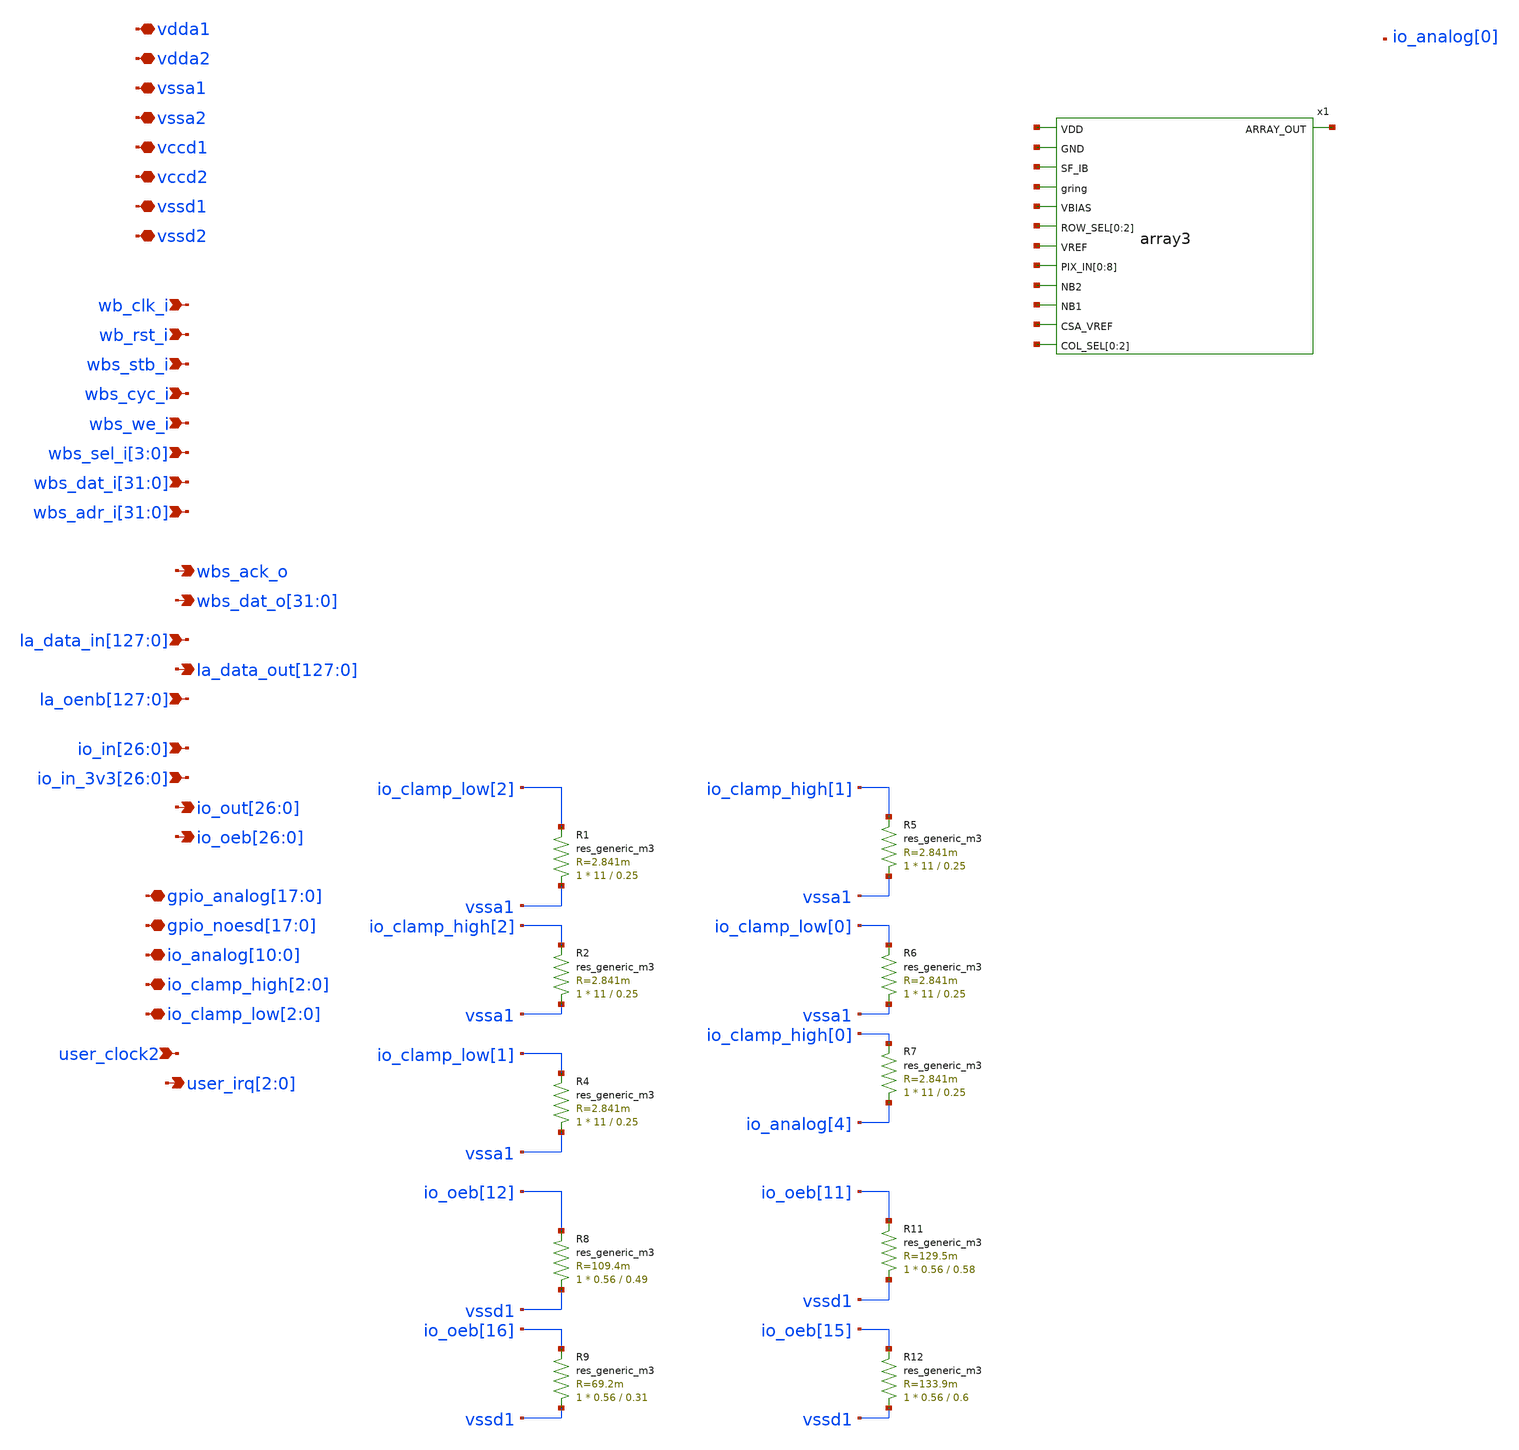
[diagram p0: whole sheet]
** sch_path: xschem/user_analog_project_wrapper.sch
**.subckt user_analog_project_wrapper vdda1 vdda2 vssa1 vssa2 vccd1 vccd2 vssd1 vssd2 wb_clk_i
*+ wb_rst_i wbs_stb_i wbs_cyc_i wbs_we_i wbs_sel_i[3],wbs_sel_i[2],wbs_sel_i[1],wbs_sel_i[0]
*+ wbs_dat_i[31],wbs_dat_i[30],wbs_dat_i[29],wbs_dat_i[28],wbs_dat_i[27],wbs_dat_i[26],wbs_dat_i[25],wbs_dat_i[24],wbs_dat_i[23],wbs_dat_i[22],wbs_dat_i[21],wbs_dat_i[20],wbs_dat_i[19],wbs_dat_i[18],wbs_dat_i[17],wbs_dat_i[16],wbs_dat_i[15],wbs_dat_i[14],wbs_dat_i[13],wbs_dat_i[12],wbs_dat_i[11],wbs_dat_i[10],wbs_dat_i[9],wbs_dat_i[8],wbs_dat_i[7],wbs_dat_i[6],wbs_dat_i[5],wbs_dat_i[4],wbs_dat_i[3],wbs_dat_i[2],wbs_dat_i[1],wbs_dat_i[0]
*+ wbs_adr_i[31],wbs_adr_i[30],wbs_adr_i[29],wbs_adr_i[28],wbs_adr_i[27],wbs_adr_i[26],wbs_adr_i[25],wbs_adr_i[24],wbs_adr_i[23],wbs_adr_i[22],wbs_adr_i[21],wbs_adr_i[20],wbs_adr_i[19],wbs_adr_i[18],wbs_adr_i[17],wbs_adr_i[16],wbs_adr_i[15],wbs_adr_i[14],wbs_adr_i[13],wbs_adr_i[12],wbs_adr_i[11],wbs_adr_i[10],wbs_adr_i[9],wbs_adr_i[8],wbs_adr_i[7],wbs_adr_i[6],wbs_adr_i[5],wbs_adr_i[4],wbs_adr_i[3],wbs_adr_i[2],wbs_adr_i[1],wbs_adr_i[0] wbs_ack_o
*+ wbs_dat_o[31],wbs_dat_o[30],wbs_dat_o[29],wbs_dat_o[28],wbs_dat_o[27],wbs_dat_o[26],wbs_dat_o[25],wbs_dat_o[24],wbs_dat_o[23],wbs_dat_o[22],wbs_dat_o[21],wbs_dat_o[20],wbs_dat_o[19],wbs_dat_o[18],wbs_dat_o[17],wbs_dat_o[16],wbs_dat_o[15],wbs_dat_o[14],wbs_dat_o[13],wbs_dat_o[12],wbs_dat_o[11],wbs_dat_o[10],wbs_dat_o[9],wbs_dat_o[8],wbs_dat_o[7],wbs_dat_o[6],wbs_dat_o[5],wbs_dat_o[4],wbs_dat_o[3],wbs_dat_o[2],wbs_dat_o[1],wbs_dat_o[0]
*+ la_data_in[127],la_data_in[126],la_data_in[125],la_data_in[124],la_data_in[123],la_data_in[122],la_data_in[121],la_data_in[120],la_data_in[119],la_data_in[118],la_data_in[117],la_data_in[116],la_data_in[115],la_data_in[114],la_data_in[113],la_data_in[112],la_data_in[111],la_data_in[110],la_data_in[109],la_data_in[108],la_data_in[107],la_data_in[106],la_data_in[105],la_data_in[104],la_data_in[103],la_data_in[102],la_data_in[101],la_data_in[100],la_data_in[99],la_data_in[98],la_data_in[97],la_data_in[96],la_data_in[95],la_data_in[94],la_data_in[93],la_data_in[92],la_data_in[91],la_data_in[90],la_data_in[89],la_data_in[88],la_data_in[87],la_data_in[86],la_data_in[85],la_data_in[84],la_data_in[83],la_data_in[82],la_data_in[81],la_data_in[80],la_data_in[79],la_data_in[78],la_data_in[77],la_data_in[76],la_data_in[75],la_data_in[74],la_data_in[73],la_data_in[72],la_data_in[71],la_data_in[70],la_data_in[69],la_data_in[68],la_data_in[67],la_data_in[66],la_data_in[65],la_data_in[64],la_data_in[63],la_data_in[62],la_data_in[61],la_data_in[60],la_data_in[59],la_data_in[58],la_data_in[57],la_data_in[56],la_data_in[55],la_data_in[54],la_data_in[53],la_data_in[52],la_data_in[51],la_data_in[50],la_data_in[49],la_data_in[48],la_data_in[47],la_data_in[46],la_data_in[45],la_data_in[44],la_data_in[43],la_data_in[42],la_data_in[41],la_data_in[40],la_data_in[39],la_data_in[38],la_data_in[37],la_data_in[36],la_data_in[35],la_data_in[34],la_data_in[33],la_data_in[32],la_data_in[31],la_data_in[30],la_data_in[29],la_data_in[28],la_data_in[27],la_data_in[26],la_data_in[25],la_data_in[24],la_data_in[23],la_data_in[22],la_data_in[21],la_data_in[20],la_data_in[19],la_data_in[18],la_data_in[17],la_data_in[16],la_data_in[15],la_data_in[14],la_data_in[13],la_data_in[12],la_data_in[11],la_data_in[10],la_data_in[9],la_data_in[8],la_data_in[7],la_data_in[6],la_data_in[5],la_data_in[4],la_data_in[3],la_data_in[2],la_data_in[1],la_data_in[0]
*+ la_data_out[127],la_data_out[126],la_data_out[125],la_data_out[124],la_data_out[123],la_data_out[122],la_data_out[121],la_data_out[120],la_data_out[119],la_data_out[118],la_data_out[117],la_data_out[116],la_data_out[115],la_data_out[114],la_data_out[113],la_data_out[112],la_data_out[111],la_data_out[110],la_data_out[109],la_data_out[108],la_data_out[107],la_data_out[106],la_data_out[105],la_data_out[104],la_data_out[103],la_data_out[102],la_data_out[101],la_data_out[100],la_data_out[99],la_data_out[98],la_data_out[97],la_data_out[96],la_data_out[95],la_data_out[94],la_data_out[93],la_data_out[92],la_data_out[91],la_data_out[90],la_data_out[89],la_data_out[88],la_data_out[87],la_data_out[86],la_data_out[85],la_data_out[84],la_data_out[83],la_data_out[82],la_data_out[81],la_data_out[80],la_data_out[79],la_data_out[78],la_data_out[77],la_data_out[76],la_data_out[75],la_data_out[74],la_data_out[73],la_data_out[72],la_data_out[71],la_data_out[70],la_data_out[69],la_data_out[68],la_data_out[67],la_data_out[66],la_data_out[65],la_data_out[64],la_data_out[63],la_data_out[62],la_data_out[61],la_data_out[60],la_data_out[59],la_data_out[58],la_data_out[57],la_data_out[56],la_data_out[55],la_data_out[54],la_data_out[53],la_data_out[52],la_data_out[51],la_data_out[50],la_data_out[49],la_data_out[48],la_data_out[47],la_data_out[46],la_data_out[45],la_data_out[44],la_data_out[43],la_data_out[42],la_data_out[41],la_data_out[40],la_data_out[39],la_data_out[38],la_data_out[37],la_data_out[36],la_data_out[35],la_data_out[34],la_data_out[33],la_data_out[32],la_data_out[31],la_data_out[30],la_data_out[29],la_data_out[28],la_data_out[27],la_data_out[26],la_data_out[25],la_data_out[24],la_data_out[23],la_data_out[22],la_data_out[21],la_data_out[20],la_data_out[19],la_data_out[18],la_data_out[17],la_data_out[16],la_data_out[15],la_data_out[14],la_data_out[13],la_data_out[12],la_data_out[11],la_data_out[10],la_data_out[9],la_data_out[8],la_data_out[7],la_data_out[6],la_data_out[5],la_data_out[4],la_data_out[3],la_data_out[2],la_data_out[1],la_data_out[0]
*+ io_in[26],io_in[25],io_in[24],io_in[23],io_in[22],io_in[21],io_in[20],io_in[19],io_in[18],io_in[17],io_in[16],io_in[15],io_in[14],io_in[13],io_in[12],io_in[11],io_in[10],io_in[9],io_in[8],io_in[7],io_in[6],io_in[5],io_in[4],io_in[3],io_in[2],io_in[1],io_in[0]
*+ io_in_3v3[26],io_in_3v3[25],io_in_3v3[24],io_in_3v3[23],io_in_3v3[22],io_in_3v3[21],io_in_3v3[20],io_in_3v3[19],io_in_3v3[18],io_in_3v3[17],io_in_3v3[16],io_in_3v3[15],io_in_3v3[14],io_in_3v3[13],io_in_3v3[12],io_in_3v3[11],io_in_3v3[10],io_in_3v3[9],io_in_3v3[8],io_in_3v3[7],io_in_3v3[6],io_in_3v3[5],io_in_3v3[4],io_in_3v3[3],io_in_3v3[2],io_in_3v3[1],io_in_3v3[0] user_clock2
*+ io_out[26],io_out[25],io_out[24],io_out[23],io_out[22],io_out[21],io_out[20],io_out[19],io_out[18],io_out[17],io_out[16],io_out[15],io_out[14],io_out[13],io_out[12],io_out[11],io_out[10],io_out[9],io_out[8],io_out[7],io_out[6],io_out[5],io_out[4],io_out[3],io_out[2],io_out[1],io_out[0]
*+ io_oeb[26],io_oeb[25],io_oeb[24],io_oeb[23],io_oeb[22],io_oeb[21],io_oeb[20],io_oeb[19],io_oeb[18],io_oeb[17],io_oeb[16],io_oeb[15],io_oeb[14],io_oeb[13],io_oeb[12],io_oeb[11],io_oeb[10],io_oeb[9],io_oeb[8],io_oeb[7],io_oeb[6],io_oeb[5],io_oeb[4],io_oeb[3],io_oeb[2],io_oeb[1],io_oeb[0]
*+ gpio_analog[17],gpio_analog[16],gpio_analog[15],gpio_analog[14],gpio_analog[13],gpio_analog[12],gpio_analog[11],gpio_analog[10],gpio_analog[9],gpio_analog[8],gpio_analog[7],gpio_analog[6],gpio_analog[5],gpio_analog[4],gpio_analog[3],gpio_analog[2],gpio_analog[1],gpio_analog[0]
*+ gpio_noesd[17],gpio_noesd[16],gpio_noesd[15],gpio_noesd[14],gpio_noesd[13],gpio_noesd[12],gpio_noesd[11],gpio_noesd[10],gpio_noesd[9],gpio_noesd[8],gpio_noesd[7],gpio_noesd[6],gpio_noesd[5],gpio_noesd[4],gpio_noesd[3],gpio_noesd[2],gpio_noesd[1],gpio_noesd[0]
*+ io_analog[10],io_analog[9],io_analog[8],io_analog[7],io_analog[6],io_analog[5],io_analog[4],io_analog[3],io_analog[2],io_analog[1],io_analog[0] io_clamp_high[2],io_clamp_high[1],io_clamp_high[0] io_clamp_low[2],io_clamp_low[1],io_clamp_low[0]
*+ user_irq[2],user_irq[1],user_irq[0]
*+ la_oenb[127],la_oenb[126],la_oenb[125],la_oenb[124],la_oenb[123],la_oenb[122],la_oenb[121],la_oenb[120],la_oenb[119],la_oenb[118],la_oenb[117],la_oenb[116],la_oenb[115],la_oenb[114],la_oenb[113],la_oenb[112],la_oenb[111],la_oenb[110],la_oenb[109],la_oenb[108],la_oenb[107],la_oenb[106],la_oenb[105],la_oenb[104],la_oenb[103],la_oenb[102],la_oenb[101],la_oenb[100],la_oenb[99],la_oenb[98],la_oenb[97],la_oenb[96],la_oenb[95],la_oenb[94],la_oenb[93],la_oenb[92],la_oenb[91],la_oenb[90],la_oenb[89],la_oenb[88],la_oenb[87],la_oenb[86],la_oenb[85],la_oenb[84],la_oenb[83],la_oenb[82],la_oenb[81],la_oenb[80],la_oenb[79],la_oenb[78],la_oenb[77],la_oenb[76],la_oenb[75],la_oenb[74],la_oenb[73],la_oenb[72],la_oenb[71],la_oenb[70],la_oenb[69],la_oenb[68],la_oenb[67],la_oenb[66],la_oenb[65],la_oenb[64],la_oenb[63],la_oenb[62],la_oenb[61],la_oenb[60],la_oenb[59],la_oenb[58],la_oenb[57],la_oenb[56],la_oenb[55],la_oenb[54],la_oenb[53],la_oenb[52],la_oenb[51],la_oenb[50],la_oenb[49],la_oenb[48],la_oenb[47],la_oenb[46],la_oenb[45],la_oenb[44],la_oenb[43],la_oenb[42],la_oenb[41],la_oenb[40],la_oenb[39],la_oenb[38],la_oenb[37],la_oenb[36],la_oenb[35],la_oenb[34],la_oenb[33],la_oenb[32],la_oenb[31],la_oenb[30],la_oenb[29],la_oenb[28],la_oenb[27],la_oenb[26],la_oenb[25],la_oenb[24],la_oenb[23],la_oenb[22],la_oenb[21],la_oenb[20],la_oenb[19],la_oenb[18],la_oenb[17],la_oenb[16],la_oenb[15],la_oenb[14],la_oenb[13],la_oenb[12],la_oenb[11],la_oenb[10],la_oenb[9],la_oenb[8],la_oenb[7],la_oenb[6],la_oenb[5],la_oenb[4],la_oenb[3],la_oenb[2],la_oenb[1],la_oenb[0]
*.iopin vdda1
*.iopin vdda2
*.iopin vssa1
*.iopin vssa2
*.iopin vccd1
*.iopin vccd2
*.iopin vssd1
*.iopin vssd2
*.ipin wb_clk_i
*.ipin wb_rst_i
*.ipin wbs_stb_i
*.ipin wbs_cyc_i
*.ipin wbs_we_i
*.ipin wbs_sel_i[3],wbs_sel_i[2],wbs_sel_i[1],wbs_sel_i[0]
*.ipin
*+ wbs_dat_i[31],wbs_dat_i[30],wbs_dat_i[29],wbs_dat_i[28],wbs_dat_i[27],wbs_dat_i[26],wbs_dat_i[25],wbs_dat_i[24],wbs_dat_i[23],wbs_dat_i[22],wbs_dat_i[21],wbs_dat_i[20],wbs_dat_i[19],wbs_dat_i[18],wbs_dat_i[17],wbs_dat_i[16],wbs_dat_i[15],wbs_dat_i[14],wbs_dat_i[13],wbs_dat_i[12],wbs_dat_i[11],wbs_dat_i[10],wbs_dat_i[9],wbs_dat_i[8],wbs_dat_i[7],wbs_dat_i[6],wbs_dat_i[5],wbs_dat_i[4],wbs_dat_i[3],wbs_dat_i[2],wbs_dat_i[1],wbs_dat_i[0]
*.ipin
*+ wbs_adr_i[31],wbs_adr_i[30],wbs_adr_i[29],wbs_adr_i[28],wbs_adr_i[27],wbs_adr_i[26],wbs_adr_i[25],wbs_adr_i[24],wbs_adr_i[23],wbs_adr_i[22],wbs_adr_i[21],wbs_adr_i[20],wbs_adr_i[19],wbs_adr_i[18],wbs_adr_i[17],wbs_adr_i[16],wbs_adr_i[15],wbs_adr_i[14],wbs_adr_i[13],wbs_adr_i[12],wbs_adr_i[11],wbs_adr_i[10],wbs_adr_i[9],wbs_adr_i[8],wbs_adr_i[7],wbs_adr_i[6],wbs_adr_i[5],wbs_adr_i[4],wbs_adr_i[3],wbs_adr_i[2],wbs_adr_i[1],wbs_adr_i[0]
*.opin wbs_ack_o
*.opin
*+ wbs_dat_o[31],wbs_dat_o[30],wbs_dat_o[29],wbs_dat_o[28],wbs_dat_o[27],wbs_dat_o[26],wbs_dat_o[25],wbs_dat_o[24],wbs_dat_o[23],wbs_dat_o[22],wbs_dat_o[21],wbs_dat_o[20],wbs_dat_o[19],wbs_dat_o[18],wbs_dat_o[17],wbs_dat_o[16],wbs_dat_o[15],wbs_dat_o[14],wbs_dat_o[13],wbs_dat_o[12],wbs_dat_o[11],wbs_dat_o[10],wbs_dat_o[9],wbs_dat_o[8],wbs_dat_o[7],wbs_dat_o[6],wbs_dat_o[5],wbs_dat_o[4],wbs_dat_o[3],wbs_dat_o[2],wbs_dat_o[1],wbs_dat_o[0]
*.ipin
*+ la_data_in[127],la_data_in[126],la_data_in[125],la_data_in[124],la_data_in[123],la_data_in[122],la_data_in[121],la_data_in[120],la_data_in[119],la_data_in[118],la_data_in[117],la_data_in[116],la_data_in[115],la_data_in[114],la_data_in[113],la_data_in[112],la_data_in[111],la_data_in[110],la_data_in[109],la_data_in[108],la_data_in[107],la_data_in[106],la_data_in[105],la_data_in[104],la_data_in[103],la_data_in[102],la_data_in[101],la_data_in[100],la_data_in[99],la_data_in[98],la_data_in[97],la_data_in[96],la_data_in[95],la_data_in[94],la_data_in[93],la_data_in[92],la_data_in[91],la_data_in[90],la_data_in[89],la_data_in[88],la_data_in[87],la_data_in[86],la_data_in[85],la_data_in[84],la_data_in[83],la_data_in[82],la_data_in[81],la_data_in[80],la_data_in[79],la_data_in[78],la_data_in[77],la_data_in[76],la_data_in[75],la_data_in[74],la_data_in[73],la_data_in[72],la_data_in[71],la_data_in[70],la_data_in[69],la_data_in[68],la_data_in[67],la_data_in[66],la_data_in[65],la_data_in[64],la_data_in[63],la_data_in[62],la_data_in[61],la_data_in[60],la_data_in[59],la_data_in[58],la_data_in[57],la_data_in[56],la_data_in[55],la_data_in[54],la_data_in[53],la_data_in[52],la_data_in[51],la_data_in[50],la_data_in[49],la_data_in[48],la_data_in[47],la_data_in[46],la_data_in[45],la_data_in[44],la_data_in[43],la_data_in[42],la_data_in[41],la_data_in[40],la_data_in[39],la_data_in[38],la_data_in[37],la_data_in[36],la_data_in[35],la_data_in[34],la_data_in[33],la_data_in[32],la_data_in[31],la_data_in[30],la_data_in[29],la_data_in[28],la_data_in[27],la_data_in[26],la_data_in[25],la_data_in[24],la_data_in[23],la_data_in[22],la_data_in[21],la_data_in[20],la_data_in[19],la_data_in[18],la_data_in[17],la_data_in[16],la_data_in[15],la_data_in[14],la_data_in[13],la_data_in[12],la_data_in[11],la_data_in[10],la_data_in[9],la_data_in[8],la_data_in[7],la_data_in[6],la_data_in[5],la_data_in[4],la_data_in[3],la_data_in[2],la_data_in[1],la_data_in[0]
*.opin
*+ la_data_out[127],la_data_out[126],la_data_out[125],la_data_out[124],la_data_out[123],la_data_out[122],la_data_out[121],la_data_out[120],la_data_out[119],la_data_out[118],la_data_out[117],la_data_out[116],la_data_out[115],la_data_out[114],la_data_out[113],la_data_out[112],la_data_out[111],la_data_out[110],la_data_out[109],la_data_out[108],la_data_out[107],la_data_out[106],la_data_out[105],la_data_out[104],la_data_out[103],la_data_out[102],la_data_out[101],la_data_out[100],la_data_out[99],la_data_out[98],la_data_out[97],la_data_out[96],la_data_out[95],la_data_out[94],la_data_out[93],la_data_out[92],la_data_out[91],la_data_out[90],la_data_out[89],la_data_out[88],la_data_out[87],la_data_out[86],la_data_out[85],la_data_out[84],la_data_out[83],la_data_out[82],la_data_out[81],la_data_out[80],la_data_out[79],la_data_out[78],la_data_out[77],la_data_out[76],la_data_out[75],la_data_out[74],la_data_out[73],la_data_out[72],la_data_out[71],la_data_out[70],la_data_out[69],la_data_out[68],la_data_out[67],la_data_out[66],la_data_out[65],la_data_out[64],la_data_out[63],la_data_out[62],la_data_out[61],la_data_out[60],la_data_out[59],la_data_out[58],la_data_out[57],la_data_out[56],la_data_out[55],la_data_out[54],la_data_out[53],la_data_out[52],la_data_out[51],la_data_out[50],la_data_out[49],la_data_out[48],la_data_out[47],la_data_out[46],la_data_out[45],la_data_out[44],la_data_out[43],la_data_out[42],la_data_out[41],la_data_out[40],la_data_out[39],la_data_out[38],la_data_out[37],la_data_out[36],la_data_out[35],la_data_out[34],la_data_out[33],la_data_out[32],la_data_out[31],la_data_out[30],la_data_out[29],la_data_out[28],la_data_out[27],la_data_out[26],la_data_out[25],la_data_out[24],la_data_out[23],la_data_out[22],la_data_out[21],la_data_out[20],la_data_out[19],la_data_out[18],la_data_out[17],la_data_out[16],la_data_out[15],la_data_out[14],la_data_out[13],la_data_out[12],la_data_out[11],la_data_out[10],la_data_out[9],la_data_out[8],la_data_out[7],la_data_out[6],la_data_out[5],la_data_out[4],la_data_out[3],la_data_out[2],la_data_out[1],la_data_out[0]
*.ipin
*+ io_in[26],io_in[25],io_in[24],io_in[23],io_in[22],io_in[21],io_in[20],io_in[19],io_in[18],io_in[17],io_in[16],io_in[15],io_in[14],io_in[13],io_in[12],io_in[11],io_in[10],io_in[9],io_in[8],io_in[7],io_in[6],io_in[5],io_in[4],io_in[3],io_in[2],io_in[1],io_in[0]
*.ipin
*+ io_in_3v3[26],io_in_3v3[25],io_in_3v3[24],io_in_3v3[23],io_in_3v3[22],io_in_3v3[21],io_in_3v3[20],io_in_3v3[19],io_in_3v3[18],io_in_3v3[17],io_in_3v3[16],io_in_3v3[15],io_in_3v3[14],io_in_3v3[13],io_in_3v3[12],io_in_3v3[11],io_in_3v3[10],io_in_3v3[9],io_in_3v3[8],io_in_3v3[7],io_in_3v3[6],io_in_3v3[5],io_in_3v3[4],io_in_3v3[3],io_in_3v3[2],io_in_3v3[1],io_in_3v3[0]
*.ipin user_clock2
*.opin
*+ io_out[26],io_out[25],io_out[24],io_out[23],io_out[22],io_out[21],io_out[20],io_out[19],io_out[18],io_out[17],io_out[16],io_out[15],io_out[14],io_out[13],io_out[12],io_out[11],io_out[10],io_out[9],io_out[8],io_out[7],io_out[6],io_out[5],io_out[4],io_out[3],io_out[2],io_out[1],io_out[0]
*.opin
*+ io_oeb[26],io_oeb[25],io_oeb[24],io_oeb[23],io_oeb[22],io_oeb[21],io_oeb[20],io_oeb[19],io_oeb[18],io_oeb[17],io_oeb[16],io_oeb[15],io_oeb[14],io_oeb[13],io_oeb[12],io_oeb[11],io_oeb[10],io_oeb[9],io_oeb[8],io_oeb[7],io_oeb[6],io_oeb[5],io_oeb[4],io_oeb[3],io_oeb[2],io_oeb[1],io_oeb[0]
*.iopin
*+ gpio_analog[17],gpio_analog[16],gpio_analog[15],gpio_analog[14],gpio_analog[13],gpio_analog[12],gpio_analog[11],gpio_analog[10],gpio_analog[9],gpio_analog[8],gpio_analog[7],gpio_analog[6],gpio_analog[5],gpio_analog[4],gpio_analog[3],gpio_analog[2],gpio_analog[1],gpio_analog[0]
*.iopin
*+ gpio_noesd[17],gpio_noesd[16],gpio_noesd[15],gpio_noesd[14],gpio_noesd[13],gpio_noesd[12],gpio_noesd[11],gpio_noesd[10],gpio_noesd[9],gpio_noesd[8],gpio_noesd[7],gpio_noesd[6],gpio_noesd[5],gpio_noesd[4],gpio_noesd[3],gpio_noesd[2],gpio_noesd[1],gpio_noesd[0]
*.iopin
*+ io_analog[10],io_analog[9],io_analog[8],io_analog[7],io_analog[6],io_analog[5],io_analog[4],io_analog[3],io_analog[2],io_analog[1],io_analog[0]
*.iopin io_clamp_high[2],io_clamp_high[1],io_clamp_high[0]
*.iopin io_clamp_low[2],io_clamp_low[1],io_clamp_low[0]
*.opin user_irq[2],user_irq[1],user_irq[0]
*.ipin
*+ la_oenb[127],la_oenb[126],la_oenb[125],la_oenb[124],la_oenb[123],la_oenb[122],la_oenb[121],la_oenb[120],la_oenb[119],la_oenb[118],la_oenb[117],la_oenb[116],la_oenb[115],la_oenb[114],la_oenb[113],la_oenb[112],la_oenb[111],la_oenb[110],la_oenb[109],la_oenb[108],la_oenb[107],la_oenb[106],la_oenb[105],la_oenb[104],la_oenb[103],la_oenb[102],la_oenb[101],la_oenb[100],la_oenb[99],la_oenb[98],la_oenb[97],la_oenb[96],la_oenb[95],la_oenb[94],la_oenb[93],la_oenb[92],la_oenb[91],la_oenb[90],la_oenb[89],la_oenb[88],la_oenb[87],la_oenb[86],la_oenb[85],la_oenb[84],la_oenb[83],la_oenb[82],la_oenb[81],la_oenb[80],la_oenb[79],la_oenb[78],la_oenb[77],la_oenb[76],la_oenb[75],la_oenb[74],la_oenb[73],la_oenb[72],la_oenb[71],la_oenb[70],la_oenb[69],la_oenb[68],la_oenb[67],la_oenb[66],la_oenb[65],la_oenb[64],la_oenb[63],la_oenb[62],la_oenb[61],la_oenb[60],la_oenb[59],la_oenb[58],la_oenb[57],la_oenb[56],la_oenb[55],la_oenb[54],la_oenb[53],la_oenb[52],la_oenb[51],la_oenb[50],la_oenb[49],la_oenb[48],la_oenb[47],la_oenb[46],la_oenb[45],la_oenb[44],la_oenb[43],la_oenb[42],la_oenb[41],la_oenb[40],la_oenb[39],la_oenb[38],la_oenb[37],la_oenb[36],la_oenb[35],la_oenb[34],la_oenb[33],la_oenb[32],la_oenb[31],la_oenb[30],la_oenb[29],la_oenb[28],la_oenb[27],la_oenb[26],la_oenb[25],la_oenb[24],la_oenb[23],la_oenb[22],la_oenb[21],la_oenb[20],la_oenb[19],la_oenb[18],la_oenb[17],la_oenb[16],la_oenb[15],la_oenb[14],la_oenb[13],la_oenb[12],la_oenb[11],la_oenb[10],la_oenb[9],la_oenb[8],la_oenb[7],la_oenb[6],la_oenb[5],la_oenb[4],la_oenb[3],la_oenb[2],la_oenb[1],la_oenb[0]
R1 vssa1 io_clamp_low[2] sky130_fd_pr__res_generic_m3 W=11 L=0.25 m=1
R2 vssa1 io_clamp_high[2] sky130_fd_pr__res_generic_m3 W=11 L=0.25 m=1
R4 vssa1 io_clamp_low[1] sky130_fd_pr__res_generic_m3 W=11 L=0.25 m=1
R5 vssa1 io_clamp_high[1] sky130_fd_pr__res_generic_m3 W=11 L=0.25 m=1
R6 vssa1 io_clamp_low[0] sky130_fd_pr__res_generic_m3 W=11 L=0.25 m=1
R7 io_analog[4] io_clamp_high[0] sky130_fd_pr__res_generic_m3 W=11 L=0.25 m=1
R8 vssd1 io_oeb[12] sky130_fd_pr__res_generic_m3 W=0.56 L=0.49 m=1
R9 vssd1 io_oeb[16] sky130_fd_pr__res_generic_m3 W=0.56 L=0.31 m=1
R11 vssd1 io_oeb[11] sky130_fd_pr__res_generic_m3 W=0.56 L=0.58 m=1
R12 vssd1 io_oeb[15] sky130_fd_pr__res_generic_m3 W=0.56 L=0.6 m=1
x1 net1 net2 net3 net4 net5 net6 net7[2] net7[1] net7[0] net8 net9[8] net9[7] net9[6] net9[5]
+ net9[4] net9[3] net9[2] net9[1] net9[0] net10 net11 net12 net13[2] net13[1] net13[0] array3
**.ends

* expanding   symbol:  array3.sym # of pins=13
** sym_path: xschem/array3.sym
** sch_path: xschem/array3.sch
.subckt array3 VDD GND SF_IB gring VBIAS ARRAY_OUT ROW_SEL[0] ROW_SEL[1] ROW_SEL[2] VREF PIX_IN[0]
+ PIX_IN[1] PIX_IN[2] PIX_IN[3] PIX_IN[4] PIX_IN[5] PIX_IN[6] PIX_IN[7] PIX_IN[8] NB2 NB1 CSA_VREF COL_SEL[0]
+ COL_SEL[1] COL_SEL[2]
*.ipin VDD
*.ipin GND
*.ipin SF_IB
*.ipin gring
*.ipin VBIAS
*.opin ARRAY_OUT
*.ipin ROW_SEL[0],ROW_SEL[1],ROW_SEL[2]
*.ipin VREF
*.ipin PIX_IN[0],PIX_IN[1],PIX_IN[2],PIX_IN[3],PIX_IN[4],PIX_IN[5],PIX_IN[6],PIX_IN[7],PIX_IN[8]
*.ipin NB2
*.ipin NB1
*.ipin CSA_VREF
*.ipin COL_SEL[0],COL_SEL[1],COL_SEL[2]
xPix0 VDD GND SF_IB gring VBIAS COL_OUT[0] ROW_SEL[0] VREF PIX_IN[0] NB2 NB1 CSA_VREF pixel
xPix1 VDD GND SF_IB gring VBIAS COL_OUT[1] ROW_SEL[0] VREF PIX_IN[1] NB2 NB1 CSA_VREF pixel
xPix2 VDD GND SF_IB gring VBIAS COL_OUT[2] ROW_SEL[0] VREF PIX_IN[2] NB2 NB1 CSA_VREF pixel
xPix3 VDD GND SF_IB gring VBIAS COL_OUT[0] ROW_SEL[1] VREF PIX_IN[3] NB2 NB1 CSA_VREF pixel
xPix4 VDD GND SF_IB gring VBIAS COL_OUT[1] ROW_SEL[1] VREF PIX_IN[4] NB2 NB1 CSA_VREF pixel
xPix5 VDD GND SF_IB gring VBIAS COL_OUT[2] ROW_SEL[1] VREF PIX_IN[5] NB2 NB1 CSA_VREF pixel
xPix6 VDD GND SF_IB gring VBIAS COL_OUT[0] ROW_SEL[2] VREF PIX_IN[6] NB2 NB1 CSA_VREF pixel
xPix7 VDD GND SF_IB gring VBIAS COL_OUT[1] ROW_SEL[2] VREF PIX_IN[7] NB2 NB1 CSA_VREF pixel
xPix8 VDD GND SF_IB gring VBIAS COL_OUT[2] ROW_SEL[2] VREF PIX_IN[8] NB2 NB1 CSA_VREF pixel
XM0 COL_OUT[0] COL_SEL[0] ARRAY_OUT GND sky130_fd_pr__nfet_01v8_lvt L=2 W=8 nf=1 ad='int((nf+1)/2) * W/nf * 0.29'
+ as='int((nf+2)/2) * W/nf * 0.29' pd='2*int((nf+1)/2) * (W/nf + 0.29)' ps='2*int((nf+2)/2) * (W/nf + 0.29)'
+ nrd='0.29 / W' nrs='0.29 / W' sa=0 sb=0 sd=0 mult=1 m=1
XM1 COL_OUT[1] COL_SEL[1] ARRAY_OUT GND sky130_fd_pr__nfet_01v8_lvt L=2 W=8 nf=1 ad='int((nf+1)/2) * W/nf * 0.29'
+ as='int((nf+2)/2) * W/nf * 0.29' pd='2*int((nf+1)/2) * (W/nf + 0.29)' ps='2*int((nf+2)/2) * (W/nf + 0.29)'
+ nrd='0.29 / W' nrs='0.29 / W' sa=0 sb=0 sd=0 mult=1 m=1
XM2 COL_OUT[2] COL_SEL[2] ARRAY_OUT GND sky130_fd_pr__nfet_01v8_lvt L=2 W=8 nf=1 ad='int((nf+1)/2) * W/nf * 0.29'
+ as='int((nf+2)/2) * W/nf * 0.29' pd='2*int((nf+1)/2) * (W/nf + 0.29)' ps='2*int((nf+2)/2) * (W/nf + 0.29)'
+ nrd='0.29 / W' nrs='0.29 / W' sa=0 sb=0 sd=0 mult=1 m=1
.ends


* expanding   symbol:  pixel/pixel.sym # of pins=12
** sym_path: xschem/pixel/pixel.sym
** sch_path: xschem/pixel/pixel.sch
.subckt pixel VDD GND SF_IB gring VBIAS pix_out ROW_SEL VREF AMP_IN NB2 NB1 CSA_VREF
*.opin pix_out
*.ipin SF_IB
*.ipin ROW_SEL
*.ipin VREF
*.ipin AMP_IN
*.ipin NB1
*.ipin CSA_VREF
*.ipin VBIAS
*.ipin NB2
*.ipin VDD
*.ipin GND
*.ipin gring
XM2 net2 ROW_SEL pix_out GND sky130_fd_pr__nfet_01v8_lvt L=1 W=2 nf=1 ad='int((nf+1)/2) * W/nf * 0.29'
+ as='int((nf+2)/2) * W/nf * 0.29' pd='2*int((nf+1)/2) * (W/nf + 0.29)' ps='2*int((nf+2)/2) * (W/nf + 0.29)'
+ nrd='0.29 / W' nrs='0.29 / W' sa=0 sb=0 sd=0 mult=1 m=1
XM3 GND AMP_OUT net1 VDD sky130_fd_pr__pfet_01v8_lvt L=1 W=1 nf=1 ad='int((nf+1)/2) * W/nf * 0.29' as='int((nf+2)/2) * W/nf * 0.29'
+ pd='2*int((nf+1)/2) * (W/nf + 0.29)' ps='2*int((nf+2)/2) * (W/nf + 0.29)' nrd='0.29 / W' nrs='0.29 / W'
+ sa=0 sb=0 sd=0 mult=1 m=1
XM5 net1 SF_IB VDD VDD sky130_fd_pr__pfet_01v8_lvt L=1 W=1 nf=1 ad='int((nf+1)/2) * W/nf * 0.29' as='int((nf+2)/2) * W/nf * 0.29'
+ pd='2*int((nf+1)/2) * (W/nf + 0.29)' ps='2*int((nf+2)/2) * (W/nf + 0.29)' nrd='0.29 / W' nrs='0.29 / W'
+ sa=0 sb=0 sd=0 mult=1 m=1
XM7 VDD net1 net2 GND sky130_fd_pr__nfet_01v8_lvt L=0.15 W=1 nf=1 ad='int((nf+1)/2) * W/nf * 0.29' as='int((nf+2)/2) * W/nf * 0.29'
+ pd='2*int((nf+1)/2) * (W/nf + 0.29)' ps='2*int((nf+2)/2) * (W/nf + 0.29)' nrd='0.29 / W' nrs='0.29 / W'
+ sa=0 sb=0 sd=0 mult=1 m=1
XM1 VDD net6 AMP_OUT GND sky130_fd_pr__nfet_01v8_lvt L=1 W=1 nf=1 ad='int((nf+1)/2) * W/nf * 0.29' as='int((nf+2)/2) * W/nf * 0.29'
+ pd='2*int((nf+1)/2) * (W/nf + 0.29)' ps='2*int((nf+2)/2) * (W/nf + 0.29)' nrd='0.29 / W' nrs='0.29 / W'
+ sa=0 sb=0 sd=0 mult=1 m=1
XM8 net5 net5 net7 VDD sky130_fd_pr__pfet_01v8_lvt L=2 W=1 nf=1 ad='int((nf+1)/2) * W/nf * 0.29' as='int((nf+2)/2) * W/nf * 0.29'
+ pd='2*int((nf+1)/2) * (W/nf + 0.29)' ps='2*int((nf+2)/2) * (W/nf + 0.29)' nrd='0.29 / W' nrs='0.29 / W'
+ sa=0 sb=0 sd=0 mult=1 m=1
XM10 net8 net7 VDD VDD sky130_fd_pr__pfet_01v8_lvt L=2 W=1 nf=1 ad='int((nf+1)/2) * W/nf * 0.29' as='int((nf+2)/2) * W/nf * 0.29'
+ pd='2*int((nf+1)/2) * (W/nf + 0.29)' ps='2*int((nf+2)/2) * (W/nf + 0.29)' nrd='0.29 / W' nrs='0.29 / W'
+ sa=0 sb=0 sd=0 mult=1 m=1
XM11 net7 net7 VDD VDD sky130_fd_pr__pfet_01v8_lvt L=2 W=1 nf=1 ad='int((nf+1)/2) * W/nf * 0.29' as='int((nf+2)/2) * W/nf * 0.29'
+ pd='2*int((nf+1)/2) * (W/nf + 0.29)' ps='2*int((nf+2)/2) * (W/nf + 0.29)' nrd='0.29 / W' nrs='0.29 / W'
+ sa=0 sb=0 sd=0 mult=1 m=1
XM15 AMP_OUT NB2 GND GND sky130_fd_pr__nfet_01v8_lvt L=1.15 W=1 nf=1 ad='int((nf+1)/2) * W/nf * 0.29'
+ as='int((nf+2)/2) * W/nf * 0.29' pd='2*int((nf+1)/2) * (W/nf + 0.29)' ps='2*int((nf+2)/2) * (W/nf + 0.29)'
+ nrd='0.29 / W' nrs='0.29 / W' sa=0 sb=0 sd=0 mult=1 m=1
XM16 net4 NB1 GND GND sky130_fd_pr__nfet_01v8_lvt L=1 W=1.2 nf=1 ad='int((nf+1)/2) * W/nf * 0.29' as='int((nf+2)/2) * W/nf * 0.29'
+ pd='2*int((nf+1)/2) * (W/nf + 0.29)' ps='2*int((nf+2)/2) * (W/nf + 0.29)' nrd='0.29 / W' nrs='0.29 / W'
+ sa=0 sb=0 sd=0 mult=1 m=1
XC3 AMP_IN AMP_OUT sky130_fd_pr__cap_mim_m3_1 W=2 L=2 MF=1 m=1
XM4 net3 VREF net4 GND sky130_fd_pr__nfet_01v8_lvt L=0.15 W=7 nf=1 ad='int((nf+1)/2) * W/nf * 0.29' as='int((nf+2)/2) * W/nf * 0.29'
+ pd='2*int((nf+1)/2) * (W/nf + 0.29)' ps='2*int((nf+2)/2) * (W/nf + 0.29)' nrd='0.29 / W' nrs='0.29 / W'
+ sa=0 sb=0 sd=0 mult=1 m=1
XM6 AMP_IN CSA_VREF AMP_OUT VDD sky130_fd_pr__pfet_01v8_lvt L=7.95 W=0.42 nf=1 ad='int((nf+1)/2) * W/nf * 0.29'
+ as='int((nf+2)/2) * W/nf * 0.29' pd='2*int((nf+1)/2) * (W/nf + 0.29)' ps='2*int((nf+2)/2) * (W/nf + 0.29)'
+ nrd='0.29 / W' nrs='0.29 / W' sa=0 sb=0 sd=0 mult=1 m=1
XM9 net6 net5 net8 VDD sky130_fd_pr__pfet_01v8_lvt L=2 W=1 nf=1 ad='int((nf+1)/2) * W/nf * 0.29' as='int((nf+2)/2) * W/nf * 0.29'
+ pd='2*int((nf+1)/2) * (W/nf + 0.29)' ps='2*int((nf+2)/2) * (W/nf + 0.29)' nrd='0.29 / W' nrs='0.29 / W'
+ sa=0 sb=0 sd=0 mult=1 m=1
XM12 net5 VBIAS net3 GND sky130_fd_pr__nfet_01v8_lvt L=0.8 W=1 nf=1 ad='int((nf+1)/2) * W/nf * 0.29'
+ as='int((nf+2)/2) * W/nf * 0.29' pd='2*int((nf+1)/2) * (W/nf + 0.29)' ps='2*int((nf+2)/2) * (W/nf + 0.29)'
+ nrd='0.29 / W' nrs='0.29 / W' sa=0 sb=0 sd=0 mult=1 m=1
XM13 net9 AMP_IN net4 GND sky130_fd_pr__nfet_01v8_lvt L=0.15 W=7 nf=1 ad='int((nf+1)/2) * W/nf * 0.29'
+ as='int((nf+2)/2) * W/nf * 0.29' pd='2*int((nf+1)/2) * (W/nf + 0.29)' ps='2*int((nf+2)/2) * (W/nf + 0.29)'
+ nrd='0.29 / W' nrs='0.29 / W' sa=0 sb=0 sd=0 mult=1 m=1
XM14 net6 VBIAS net9 GND sky130_fd_pr__nfet_01v8_lvt L=0.8 W=1 nf=1 ad='int((nf+1)/2) * W/nf * 0.29'
+ as='int((nf+2)/2) * W/nf * 0.29' pd='2*int((nf+1)/2) * (W/nf + 0.29)' ps='2*int((nf+2)/2) * (W/nf + 0.29)'
+ nrd='0.29 / W' nrs='0.29 / W' sa=0 sb=0 sd=0 mult=1 m=1
XMD_4 GND GND GND GND sky130_fd_pr__nfet_01v8_lvt L=0.35 W=2.6 nf=1 ad='int((nf+1)/2) * W/nf * 0.29'
+ as='int((nf+2)/2) * W/nf * 0.29' pd='2*int((nf+1)/2) * (W/nf + 0.29)' ps='2*int((nf+2)/2) * (W/nf + 0.29)'
+ nrd='0.29 / W' nrs='0.29 / W' sa=0 sb=0 sd=0 mult=1 m=1
XMD_1 GND GND GND GND sky130_fd_pr__nfet_01v8_lvt L=2 W=2 nf=1 ad='int((nf+1)/2) * W/nf * 0.29' as='int((nf+2)/2) * W/nf * 0.29'
+ pd='2*int((nf+1)/2) * (W/nf + 0.29)' ps='2*int((nf+2)/2) * (W/nf + 0.29)' nrd='0.29 / W' nrs='0.29 / W'
+ sa=0 sb=0 sd=0 mult=1 m=1
XM17 VDD VDD VDD VDD sky130_fd_pr__pfet_01v8_lvt L=0.65 W=0.65 nf=1 ad='int((nf+1)/2) * W/nf * 0.29'
+ as='int((nf+2)/2) * W/nf * 0.29' pd='2*int((nf+1)/2) * (W/nf + 0.29)' ps='2*int((nf+2)/2) * (W/nf + 0.29)'
+ nrd='0.29 / W' nrs='0.29 / W' sa=0 sb=0 sd=0 mult=1 m=1
XMD_2 GND GND GND GND sky130_fd_pr__nfet_01v8_lvt L=3.35 W=2 nf=1 ad='int((nf+1)/2) * W/nf * 0.29' as='int((nf+2)/2) * W/nf * 0.29'
+ pd='2*int((nf+1)/2) * (W/nf + 0.29)' ps='2*int((nf+2)/2) * (W/nf + 0.29)' nrd='0.29 / W' nrs='0.29 / W'
+ sa=0 sb=0 sd=0 mult=1 m=1
.ends

.GLOBAL VDD
.GLOBAL GND
.end
